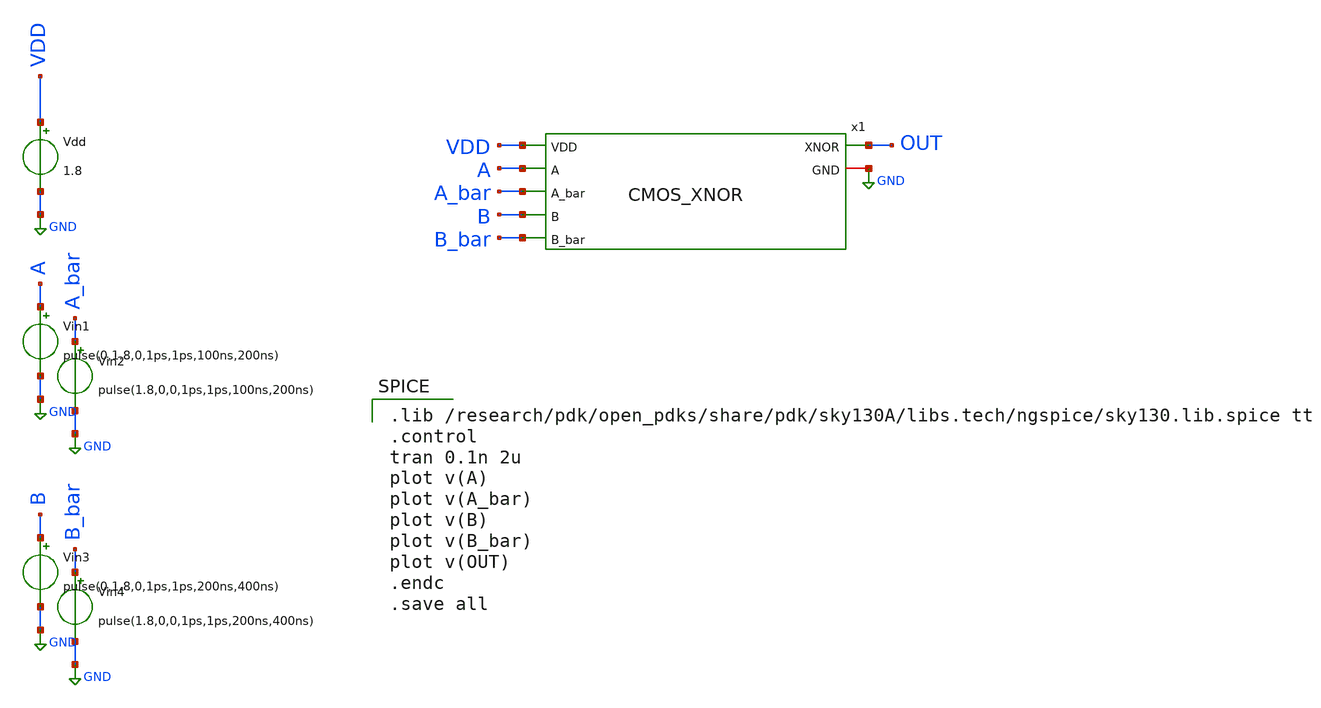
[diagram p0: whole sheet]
** sch_path: skywater_stuff/CMOS_XNOR_sim.sch
**.subckt CMOS_XNOR_sim
Vdd VDD GND 1.8
Vin1 A GND pulse(0,1.8,0,1ps,1ps,100ns,200ns)
Vin2 A_bar GND pulse(1.8,0,0,1ps,1ps,100ns,200ns)
Vin3 B GND pulse(0,1.8,0,1ps,1ps,200ns,400ns)
Vin4 B_bar GND pulse(1.8,0,0,1ps,1ps,200ns,400ns)
x1 A A_bar B B_bar OUT GND VDD CMOS_XNOR
**** begin user architecture code

.lib /research/pdk/open_pdks/share/pdk/sky130A/libs.tech/ngspice/sky130.lib.spice tt
.control
tran 0.1n 2u
plot v(A)
plot v(A_bar)
plot v(B)
plot v(B_bar)
plot v(OUT)
.endc
.save all

**** end user architecture code
**.ends

* expanding   symbol:  CMOS_XNOR.sym # of pins=7
** sym_path: skywater_stuff/CMOS_XNOR.sym
** sch_path: skywater_stuff/CMOS_XNOR.sch
.subckt CMOS_XNOR A A_bar B B_bar XNOR GND VDD
*.ipin A
*.ipin A_bar
*.ipin B
*.ipin B_bar
*.opin XNOR
*.iopin GND
*.ipin VDD
XM8 net5 A_bar GND GND sky130_fd_pr__nfet_01v8 L=0.15 W=1.5 nf=1 ad='int((nf+1)/2) * W/nf * 0.29' as='int((nf+2)/2) * W/nf * 0.29'
+ pd='2*int((nf+1)/2) * (W/nf + 0.29)' ps='2*int((nf+2)/2) * (W/nf + 0.29)' nrd='0.29 / W' nrs='0.29 / W'
+ sa=0 sb=0 sd=0 mult=1 m=1
XM1 net3 B net4 GND sky130_fd_pr__nfet_01v8 L=0.15 W=1.5 nf=1 ad='int((nf+1)/2) * W/nf * 0.29' as='int((nf+2)/2) * W/nf * 0.29'
+ pd='2*int((nf+1)/2) * (W/nf + 0.29)' ps='2*int((nf+2)/2) * (W/nf + 0.29)' nrd='0.29 / W' nrs='0.29 / W'
+ sa=0 sb=0 sd=0 mult=1 m=1
XM3 net3 A net1 VDD sky130_fd_pr__pfet_01v8 L=0.15 W=3 nf=1 ad='int((nf+1)/2) * W/nf * 0.29' as='int((nf+2)/2) * W/nf * 0.29'
+ pd='2*int((nf+1)/2) * (W/nf + 0.29)' ps='2*int((nf+2)/2) * (W/nf + 0.29)' nrd='0.29 / W' nrs='0.29 / W'
+ sa=0 sb=0 sd=0 mult=1 m=1
XM4 net2 B VDD VDD sky130_fd_pr__pfet_01v8 L=0.15 W=3 nf=1 ad='int((nf+1)/2) * W/nf * 0.29' as='int((nf+2)/2) * W/nf * 0.29'
+ pd='2*int((nf+1)/2) * (W/nf + 0.29)' ps='2*int((nf+2)/2) * (W/nf + 0.29)' nrd='0.29 / W' nrs='0.29 / W'
+ sa=0 sb=0 sd=0 mult=1 m=1
XM9 net1 B_bar VDD VDD sky130_fd_pr__pfet_01v8 L=0.15 W=3 nf=1 ad='int((nf+1)/2) * W/nf * 0.29' as='int((nf+2)/2) * W/nf * 0.29'
+ pd='2*int((nf+1)/2) * (W/nf + 0.29)' ps='2*int((nf+2)/2) * (W/nf + 0.29)' nrd='0.29 / W' nrs='0.29 / W'
+ sa=0 sb=0 sd=0 mult=1 m=1
XM2 net3 B_bar net5 GND sky130_fd_pr__nfet_01v8 L=0.15 W=1.5 nf=1 ad='int((nf+1)/2) * W/nf * 0.29' as='int((nf+2)/2) * W/nf * 0.29'
+ pd='2*int((nf+1)/2) * (W/nf + 0.29)' ps='2*int((nf+2)/2) * (W/nf + 0.29)' nrd='0.29 / W' nrs='0.29 / W'
+ sa=0 sb=0 sd=0 mult=1 m=1
XM5 net4 A GND GND sky130_fd_pr__nfet_01v8 L=0.15 W=1.5 nf=1 ad='int((nf+1)/2) * W/nf * 0.29' as='int((nf+2)/2) * W/nf * 0.29'
+ pd='2*int((nf+1)/2) * (W/nf + 0.29)' ps='2*int((nf+2)/2) * (W/nf + 0.29)' nrd='0.29 / W' nrs='0.29 / W'
+ sa=0 sb=0 sd=0 mult=1 m=1
XM10 net3 A_bar net2 VDD sky130_fd_pr__pfet_01v8 L=0.15 W=3 nf=1 ad='int((nf+1)/2) * W/nf * 0.29' as='int((nf+2)/2) * W/nf * 0.29'
+ pd='2*int((nf+1)/2) * (W/nf + 0.29)' ps='2*int((nf+2)/2) * (W/nf + 0.29)' nrd='0.29 / W' nrs='0.29 / W'
+ sa=0 sb=0 sd=0 mult=1 m=1
XM6 XNOR net3 GND GND sky130_fd_pr__nfet_01v8 L=0.15 W=1.5 nf=1 ad='int((nf+1)/2) * W/nf * 0.29' as='int((nf+2)/2) * W/nf * 0.29'
+ pd='2*int((nf+1)/2) * (W/nf + 0.29)' ps='2*int((nf+2)/2) * (W/nf + 0.29)' nrd='0.29 / W' nrs='0.29 / W'
+ sa=0 sb=0 sd=0 mult=1 m=1
XM7 XNOR net3 VDD VDD sky130_fd_pr__pfet_01v8 L=0.15 W=3 nf=1 ad='int((nf+1)/2) * W/nf * 0.29' as='int((nf+2)/2) * W/nf * 0.29'
+ pd='2*int((nf+1)/2) * (W/nf + 0.29)' ps='2*int((nf+2)/2) * (W/nf + 0.29)' nrd='0.29 / W' nrs='0.29 / W'
+ sa=0 sb=0 sd=0 mult=1 m=1
.ends

.GLOBAL GND
.end
